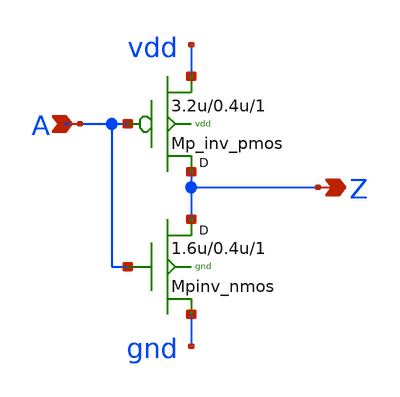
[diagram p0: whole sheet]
** sch_path: sram_2_16_scn4m/pinv_0.sch
**.subckt pinv_0 A Z
*.ipin A
*.opin Z
Mpinv_nmos Z A gnd gnd n w=1.6u l=0.4u m=1
Mp_inv_pmos Z A vdd vdd p w=3.2u l=0.4u m=1
**.ends
.end
